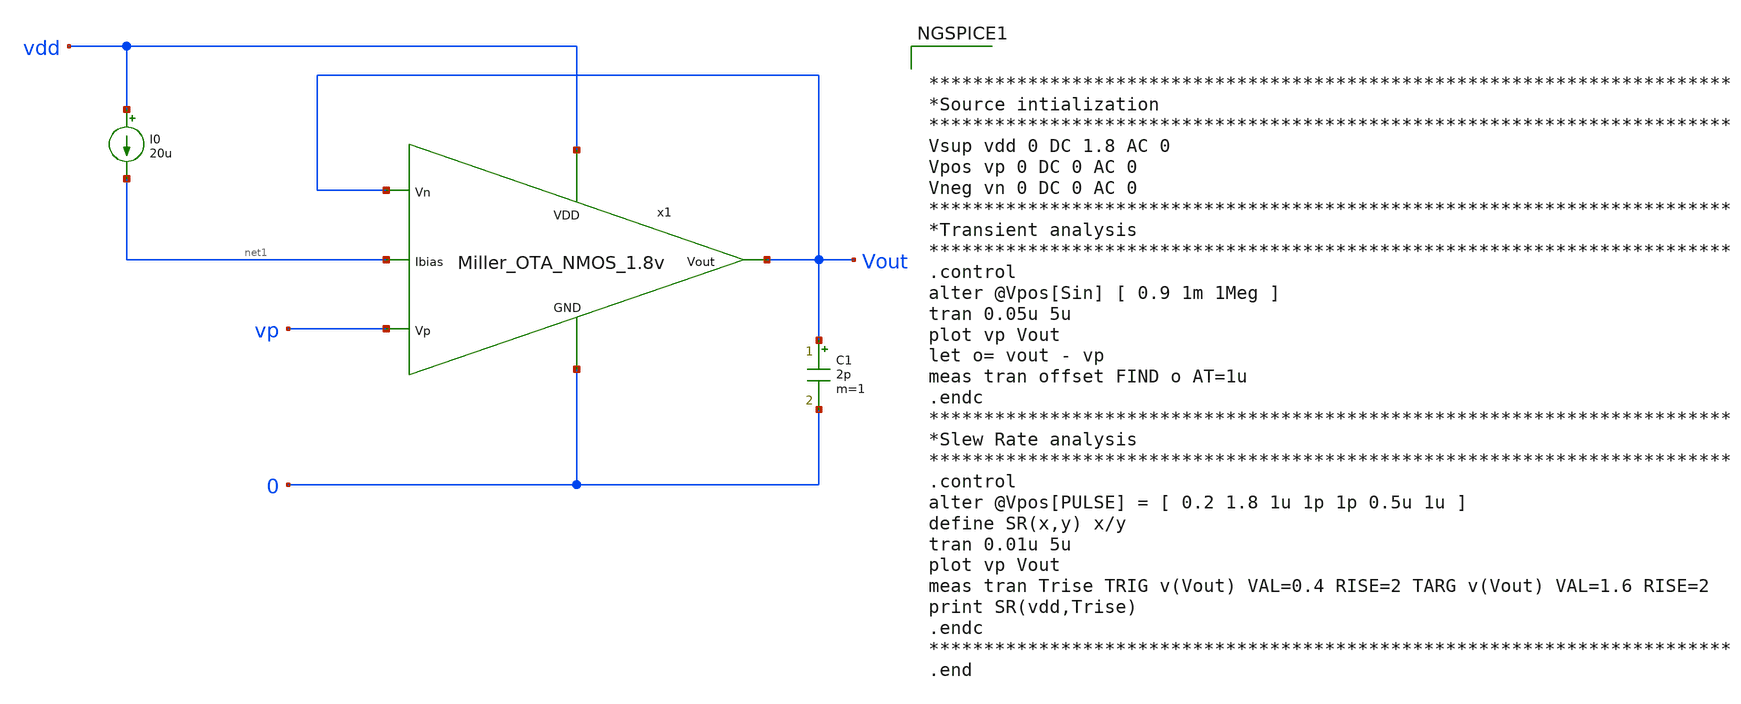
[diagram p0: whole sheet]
** sch_path: Analog_Blocks/OTA/Testbench/Miller_OTA_meas_tran.sch
**.subckt Miller_OTA_meas_tran
I0 vdd net1 20u
C1 Vout 0 2p m=1
x1 vdd Vout vp Vout net1 0 Miller_OTA_NMOS_1.8v
**** begin user architecture code

.include $::SKYWATER_MODELS/cells/nfet_01v8/sky130_fd_pr__nfet_01v8__tt.corner.spice
.include $::SKYWATER_MODELS/cells/nfet_01v8_lvt/sky130_fd_pr__nfet_01v8_lvt__tt.corner.spice
.include $::SKYWATER_MODELS/cells/pfet_01v8/sky130_fd_pr__pfet_01v8__tt.corner.spice
.include $::SKYWATER_MODELS/cells/nfet_03v3_nvt/sky130_fd_pr__nfet_03v3_nvt__tt.corner.spice
.include $::SKYWATER_MODELS/cells/nfet_05v0_nvt/sky130_fd_pr__nfet_05v0_nvt__tt.corner.spice
.include $::SKYWATER_MODELS/cells/esd_nfet_01v8/sky130_fd_pr__esd_nfet_01v8__tt.corner.spice
.include $::SKYWATER_MODELS/cells/pfet_01v8_lvt/sky130_fd_pr__pfet_01v8_lvt__tt.corner.spice
.include $::SKYWATER_MODELS/cells/pfet_01v8_hvt/sky130_fd_pr__pfet_01v8_hvt__tt.corner.spice
.include $::SKYWATER_MODELS/cells/esd_pfet_g5v0d10v5/sky130_fd_pr__esd_pfet_g5v0d10v5__tt.corner.spice
.include $::SKYWATER_MODELS/cells/pfet_g5v0d10v5/sky130_fd_pr__pfet_g5v0d10v5__tt.corner.spice
.include $::SKYWATER_MODELS/cells/pfet_g5v0d16v0/sky130_fd_pr__pfet_g5v0d16v0__tt.corner.spice
.include $::SKYWATER_MODELS/cells/nfet_g5v0d10v5/sky130_fd_pr__nfet_g5v0d10v5__tt.corner.spice
.include $::SKYWATER_MODELS/cells/nfet_g5v0d16v0/sky130_fd_pr__nfet_g5v0d16v0__tt_discrete.corner.spice
.include $::SKYWATER_MODELS/cells/esd_nfet_g5v0d10v5/sky130_fd_pr__esd_nfet_g5v0d10v5__tt.corner.spice
.include $::SKYWATER_MODELS/models/corners/tt/nonfet.spice
* Mismatch parameters
.include $::SKYWATER_MODELS/cells/nfet_01v8/sky130_fd_pr__nfet_01v8__mismatch.corner.spice
.include $::SKYWATER_MODELS/cells/pfet_01v8/sky130_fd_pr__pfet_01v8__mismatch.corner.spice
.include $::SKYWATER_MODELS/cells/nfet_01v8_lvt/sky130_fd_pr__nfet_01v8_lvt__mismatch.corner.spice
.include $::SKYWATER_MODELS/cells/pfet_01v8_lvt/sky130_fd_pr__pfet_01v8_lvt__mismatch.corner.spice
.include $::SKYWATER_MODELS/cells/pfet_01v8_hvt/sky130_fd_pr__pfet_01v8_hvt__mismatch.corner.spice
.include $::SKYWATER_MODELS/cells/nfet_g5v0d10v5/sky130_fd_pr__nfet_g5v0d10v5__mismatch.corner.spice
.include $::SKYWATER_MODELS/cells/pfet_g5v0d10v5/sky130_fd_pr__pfet_g5v0d10v5__mismatch.corner.spice
.include $::SKYWATER_MODELS/cells/nfet_05v0_nvt/sky130_fd_pr__nfet_05v0_nvt__mismatch.corner.spice
.include $::SKYWATER_MODELS/cells/nfet_03v3_nvt/sky130_fd_pr__nfet_03v3_nvt__mismatch.corner.spice
* Resistor$::SKYWATER_MODELS/Capacitor
.include $::SKYWATER_MODELS/models/r+c/res_typical__cap_typical.spice
.include $::SKYWATER_MODELS/models/r+c/res_typical__cap_typical__lin.spice
* Special cells
.include $::SKYWATER_MODELS/models/corners/tt/specialized_cells.spice
* All models
.include $::SKYWATER_MODELS/models/all.spice
* Corner
.include $::SKYWATER_MODELS/models/corners/tt/rf.spice



*************************************************************************
*Source intialization
*************************************************************************
Vsup vdd 0 DC 1.8 AC 0
Vpos vp 0 DC 0 AC 0
Vneg vn 0 DC 0 AC 0
*************************************************************************
*Transient analysis
*************************************************************************
.control
alter @Vpos[Sin] [ 0.9 1m 1Meg ]
tran 0.05u 5u
plot vp Vout
let o= vout - vp
meas tran offset FIND o AT=1u
.endc
*************************************************************************
*Slew Rate analysis
*************************************************************************
.control
alter @Vpos[PULSE] = [ 0.2 1.8 1u 1p 1p 0.5u 1u ]
define SR(x,y) x/y
tran 0.01u 5u
plot vp Vout
meas tran Trise TRIG v(Vout) VAL=0.4 RISE=2 TARG v(Vout) VAL=1.6 RISE=2
print SR(vdd,Trise)
.endc
*************************************************************************
.end


**** end user architecture code
**.ends
.end
